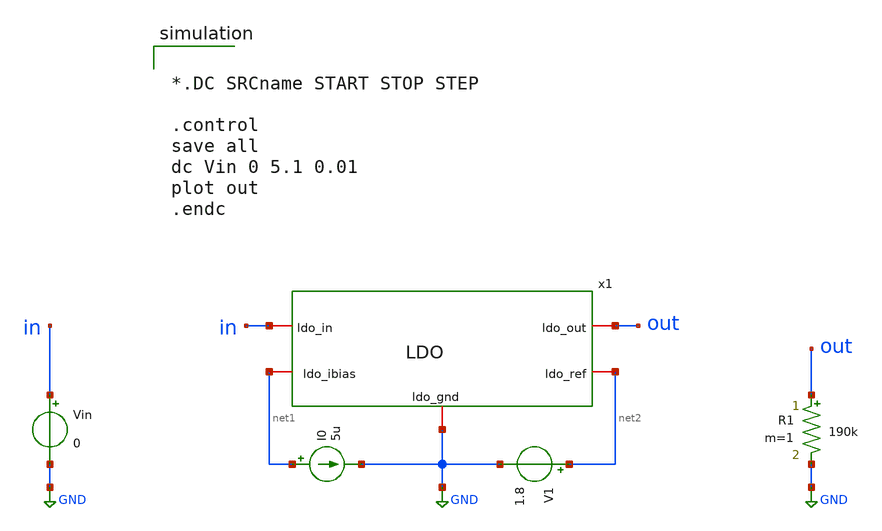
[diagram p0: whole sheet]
** sch_path: xschem/tb-LDO.sch
**.subckt tb-LDO
x1 in out net1 net2 GND LDO
I0 net1 GND 5u
V1 net2 GND 1.8
Vin in GND 0
R1 out GND 190k m=1
**** begin user architecture code

** opencircuitdesign pdks install
.lib $::SKYWATER_MODELS/sky130.lib.spice tt




*.DC SRCname START STOP STEP

.control
save all
dc Vin 0 5.1 0.01
plot out
.endc



**** end user architecture code
**.ends

* expanding   symbol:  LDO.sym # of pins=5
** sym_path: xschem/LDO.sym
** sch_path: xschem/LDO.sch
.subckt LDO ldo_in ldo_out ldo_ibias ldo_ref ldo_gnd
*.iopin ldo_out
*.iopin ldo_in
*.iopin ldo_gnd
*.iopin ldo_ref
*.iopin ldo_ibias
x1 ldo_in ldo_out ldo_ref net1 ldo_ibias ldo_gnd Ota_esq
XM1 ldo_in net1 ldo_out ldo_gnd sky130_fd_pr__nfet_03v3_nvt L=0.5 W=10 nf=1 ad='int((nf+1)/2) * W/nf * 0.29'
+ as='int((nf+2)/2) * W/nf * 0.29' pd='2*int((nf+1)/2) * (W/nf + 0.29)' ps='2*int((nf+2)/2) * (W/nf + 0.29)'
+ nrd='0.29 / W' nrs='0.29 / W' sa=0 sb=0 sd=0 mult=1 m=1
.ends


* expanding   symbol:  Ota_esq.sym # of pins=6
** sym_path: xschem/Ota_esq.sym
** sch_path: xschem/Ota_esq.sch
.subckt Ota_esq VDD Vin Vip Vout Ibias VSS
*.ipin Vin
*.ipin Vip
*.iopin VDD
*.iopin VSS
*.iopin Ibias
*.opin Vout
XC1 net2 Vout sky130_fd_pr__cap_mim_m3_1 W=23 L=23 MF=1 m=1
XM3 VSS net1 net1 VSS sky130_fd_pr__nfet_g5v0d10v5 L=0.5 W=7 nf=1 ad='int((nf+1)/2) * W/nf * 0.29' as='int((nf+2)/2) * W/nf * 0.29'
+ pd='2*int((nf+1)/2) * (W/nf + 0.29)' ps='2*int((nf+2)/2) * (W/nf + 0.29)' nrd='0.29 / W' nrs='0.29 / W'
+ sa=0 sb=0 sd=0 mult=1 m=1
XM1 net1 Vin net3 net3 sky130_fd_pr__pfet_g5v0d10v5 L=0.5 W=2 nf=1 ad='int((nf+1)/2) * W/nf * 0.29' as='int((nf+2)/2) * W/nf * 0.29'
+ pd='2*int((nf+1)/2) * (W/nf + 0.29)' ps='2*int((nf+2)/2) * (W/nf + 0.29)' nrd='0.29 / W' nrs='0.29 / W'
+ sa=0 sb=0 sd=0 mult=1 m=1
XM2 net3 Vip net2 net3 sky130_fd_pr__pfet_g5v0d10v5 L=0.5 W=2 nf=1 ad='int((nf+1)/2) * W/nf * 0.29' as='int((nf+2)/2) * W/nf * 0.29'
+ pd='2*int((nf+1)/2) * (W/nf + 0.29)' ps='2*int((nf+2)/2) * (W/nf + 0.29)' nrd='0.29 / W' nrs='0.29 / W'
+ sa=0 sb=0 sd=0 mult=1 m=1
XM4 net2 net1 VSS VSS sky130_fd_pr__nfet_g5v0d10v5 L=0.5 W=7 nf=1 ad='int((nf+1)/2) * W/nf * 0.29' as='int((nf+2)/2) * W/nf * 0.29'
+ pd='2*int((nf+1)/2) * (W/nf + 0.29)' ps='2*int((nf+2)/2) * (W/nf + 0.29)' nrd='0.29 / W' nrs='0.29 / W'
+ sa=0 sb=0 sd=0 mult=1 m=1
XM7 Vout net2 VSS VSS sky130_fd_pr__nfet_g5v0d10v5 L=1 W=21 nf=7 ad='int((nf+1)/2) * W/nf * 0.29' as='int((nf+2)/2) * W/nf * 0.29'
+ pd='2*int((nf+1)/2) * (W/nf + 0.29)' ps='2*int((nf+2)/2) * (W/nf + 0.29)' nrd='0.29 / W' nrs='0.29 / W'
+ sa=0 sb=0 sd=0 mult=1 m=1
XM8 VDD Ibias Ibias VDD sky130_fd_pr__pfet_g5v0d10v5 L=1 W=24 nf=8 ad='int((nf+1)/2) * W/nf * 0.29' as='int((nf+2)/2) * W/nf * 0.29'
+ pd='2*int((nf+1)/2) * (W/nf + 0.29)' ps='2*int((nf+2)/2) * (W/nf + 0.29)' nrd='0.29 / W' nrs='0.29 / W'
+ sa=0 sb=0 sd=0 mult=1 m=1
XM5 net3 Ibias VDD VDD sky130_fd_pr__pfet_g5v0d10v5 L=1 W=24 nf=8 ad='int((nf+1)/2) * W/nf * 0.29' as='int((nf+2)/2) * W/nf * 0.29'
+ pd='2*int((nf+1)/2) * (W/nf + 0.29)' ps='2*int((nf+2)/2) * (W/nf + 0.29)' nrd='0.29 / W' nrs='0.29 / W'
+ sa=0 sb=0 sd=0 mult=1 m=1
XM6 Vout Ibias VDD VDD sky130_fd_pr__pfet_g5v0d10v5 L=1 W=39 nf=13 ad='int((nf+1)/2) * W/nf * 0.29' as='int((nf+2)/2) * W/nf * 0.29'
+ pd='2*int((nf+1)/2) * (W/nf + 0.29)' ps='2*int((nf+2)/2) * (W/nf + 0.29)' nrd='0.29 / W' nrs='0.29 / W'
+ sa=0 sb=0 sd=0 mult=1 m=1
.ends

.GLOBAL GND
.end
